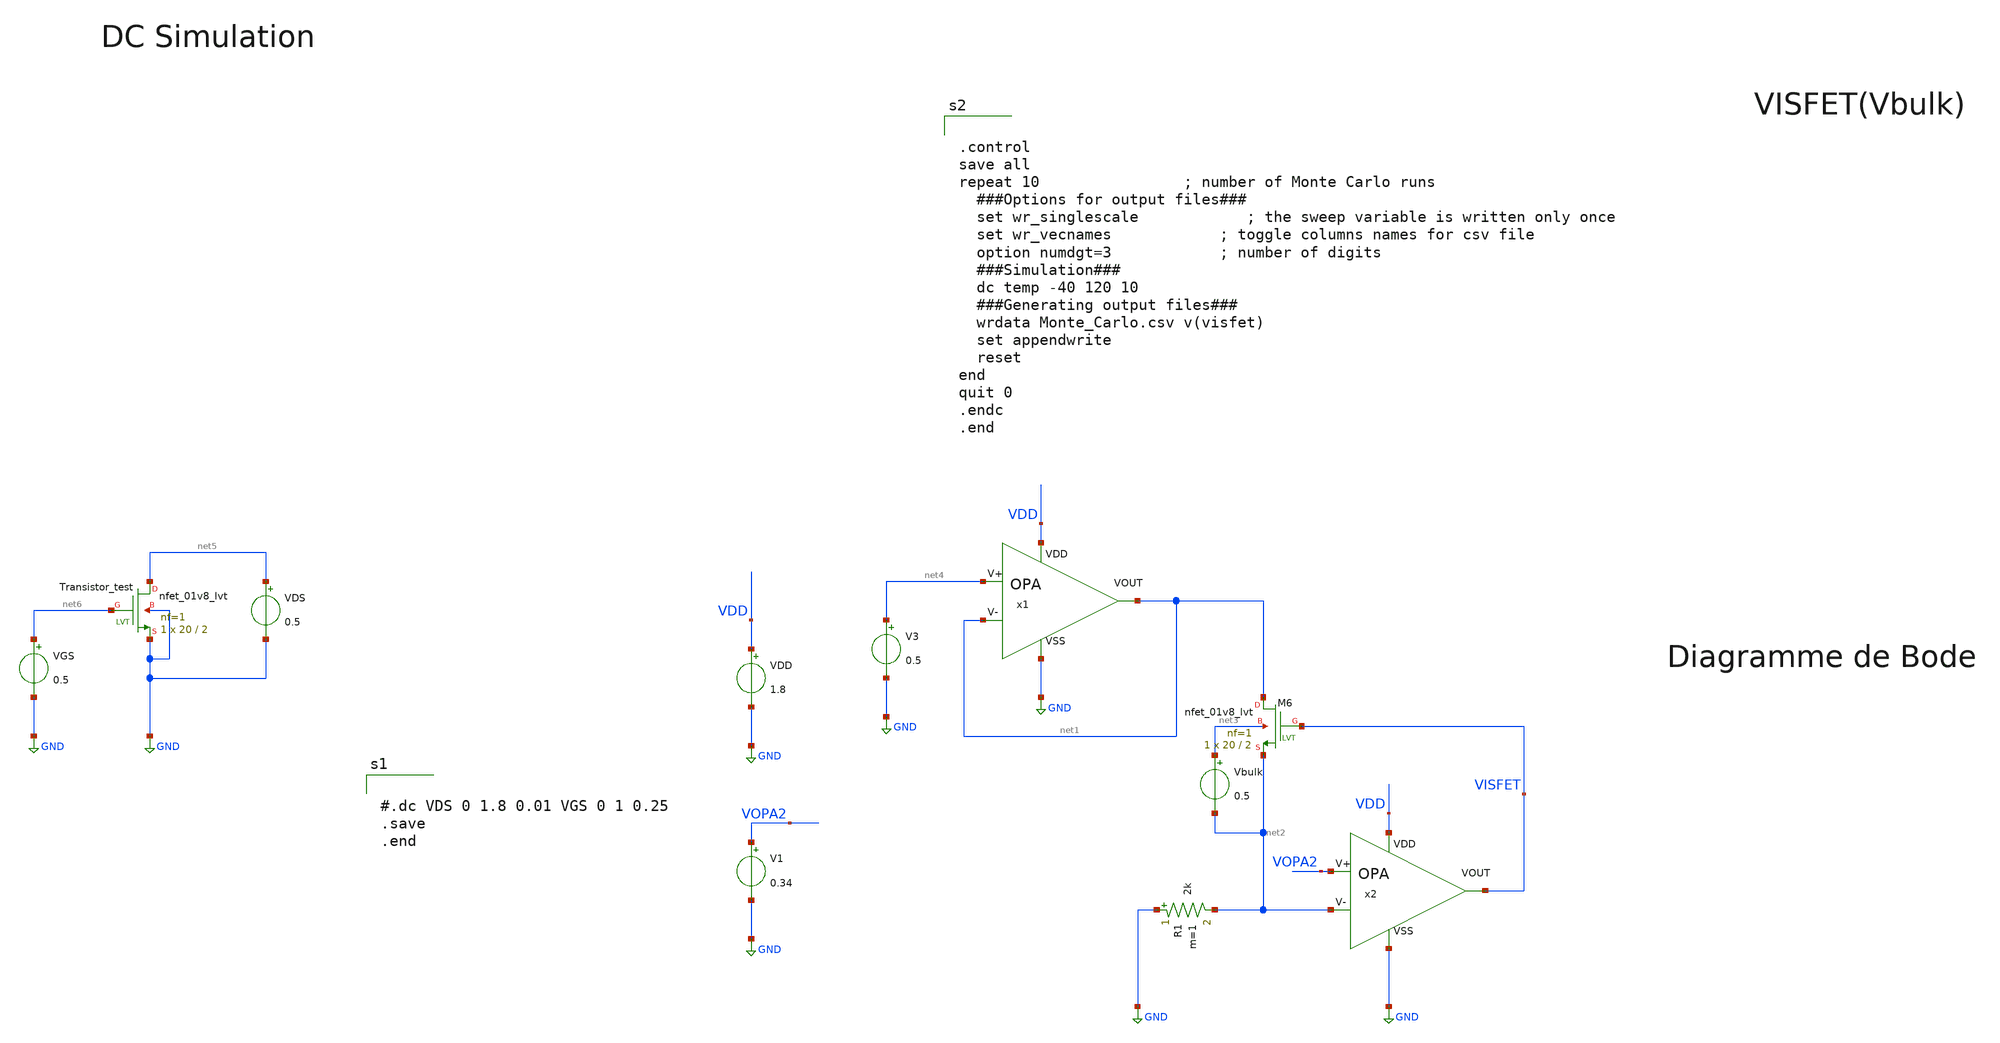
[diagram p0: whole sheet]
** sch_path: CVCC.sch
**.subckt CVCC
XM6 net1 VISFET net2 net3 sky130_fd_pr__nfet_01v8_lvt L=2 W=20 nf=1 ad='int((nf+1)/2) * W/nf * 0.29'
+ as='int((nf+2)/2) * W/nf * 0.29' pd='2*int((nf+1)/2) * (W/nf + 0.29)' ps='2*int((nf+2)/2) * (W/nf + 0.29)'
+ nrd='0.29 / W' nrs='0.29 / W' sa=0 sb=0 sd=0 mult=1 m=1
V1 VOPA2 GND 0.34
x1 VDD net4 net1 net1 GND OPA
x2 VDD VOPA2 net2 VISFET GND OPA
R1 GND net2 2k m=1
Vbulk net3 net2 0.5
VDD VDD GND 1.8
XTransistor_test net5 net6 GND GND sky130_fd_pr__nfet_01v8_lvt L=2 W=20 nf=1 ad='int((nf+1)/2) * W/nf * 0.29'
+ as='int((nf+2)/2) * W/nf * 0.29' pd='2*int((nf+1)/2) * (W/nf + 0.29)' ps='2*int((nf+2)/2) * (W/nf + 0.29)'
+ nrd='0.29 / W' nrs='0.29 / W' sa=0 sb=0 sd=0 mult=1 m=1
VDS net5 GND 0.5
VGS net6 GND 0.5
V3 net4 GND 0.5
**** begin user architecture code

** opencircuitdesign pdks install
.param MC_SWITCH=1.0
.lib $::SKYWATER_MODELS/sky130.lib.spice tt



#.dc VDS 0 1.8 0.01 VGS 0 1 0.25
.save
.end



.control
save all
repeat 10				; number of Monte Carlo runs
  ###Options for output files###
  set wr_singlescale			; the sweep variable is written only once
  set wr_vecnames			; toggle columns names for csv file
  option numdgt=3			; number of digits
  ###Simulation###
  dc temp -40 120 10
  ###Generating output files###
  wrdata Monte_Carlo.csv v(visfet)
  set appendwrite
  reset
end
quit 0
.endc
.end

**** end user architecture code
**.ends

* expanding   symbol:  OPA.sym # of pins=5
** sym_path: OPA.sym
** sch_path: OPA.sch
.subckt OPA VDD V+ V- VOUT VSS
*.ipin VSS
*.opin VOUT
*.ipin VDD
*.ipin V-
*.ipin V+
XM16 net5 net5 VDD VDD sky130_fd_pr__pfet_01v8_lvt L=2 W=39.5 nf=1 ad='int((nf+1)/2) * W/nf * 0.29' as='int((nf+2)/2) * W/nf * 0.29'
+ pd='2*int((nf+1)/2) * (W/nf + 0.29)' ps='2*int((nf+2)/2) * (W/nf + 0.29)' nrd='0.29 / W' nrs='0.29 / W'
+ sa=0 sb=0 sd=0 mult=1 m=1
XM17 net4 net4 net5 net5 sky130_fd_pr__pfet_01v8_lvt L=2 W=39.5 nf=1 ad='int((nf+1)/2) * W/nf * 0.29'
+ as='int((nf+2)/2) * W/nf * 0.29' pd='2*int((nf+1)/2) * (W/nf + 0.29)' ps='2*int((nf+2)/2) * (W/nf + 0.29)'
+ nrd='0.29 / W' nrs='0.29 / W' sa=0 sb=0 sd=0 mult=1 m=1
XM18 net4 net4 VSS VSS sky130_fd_pr__nfet_01v8_lvt L=2 W=6.67 nf=1 ad='int((nf+1)/2) * W/nf * 0.29' as='int((nf+2)/2) * W/nf * 0.29'
+ pd='2*int((nf+1)/2) * (W/nf + 0.29)' ps='2*int((nf+2)/2) * (W/nf + 0.29)' nrd='0.29 / W' nrs='0.29 / W'
+ sa=0 sb=0 sd=0 mult=1 m=1
XM19 net2 net4 VSS VSS sky130_fd_pr__nfet_01v8_lvt L=2 W=20 nf=1 ad='int((nf+1)/2) * W/nf * 0.29' as='int((nf+2)/2) * W/nf * 0.29'
+ pd='2*int((nf+1)/2) * (W/nf + 0.29)' ps='2*int((nf+2)/2) * (W/nf + 0.29)' nrd='0.29 / W' nrs='0.29 / W'
+ sa=0 sb=0 sd=0 mult=1 m=1
XM1 net1 V- net2 GND sky130_fd_pr__nfet_01v8_lvt L=2 W=10 nf=1 ad='int((nf+1)/2) * W/nf * 0.29' as='int((nf+2)/2) * W/nf * 0.29'
+ pd='2*int((nf+1)/2) * (W/nf + 0.29)' ps='2*int((nf+2)/2) * (W/nf + 0.29)' nrd='0.29 / W' nrs='0.29 / W'
+ sa=0 sb=0 sd=0 mult=1 m=1
XM2 net3 V+ net2 GND sky130_fd_pr__nfet_01v8_lvt L=2 W=10 nf=1 ad='int((nf+1)/2) * W/nf * 0.29' as='int((nf+2)/2) * W/nf * 0.29'
+ pd='2*int((nf+1)/2) * (W/nf + 0.29)' ps='2*int((nf+2)/2) * (W/nf + 0.29)' nrd='0.29 / W' nrs='0.29 / W'
+ sa=0 sb=0 sd=0 mult=1 m=1
XM3 net3 net1 VDD VDD sky130_fd_pr__pfet_01v8_lvt L=2 W=59.25 nf=1 ad='int((nf+1)/2) * W/nf * 0.29' as='int((nf+2)/2) * W/nf * 0.29'
+ pd='2*int((nf+1)/2) * (W/nf + 0.29)' ps='2*int((nf+2)/2) * (W/nf + 0.29)' nrd='0.29 / W' nrs='0.29 / W'
+ sa=0 sb=0 sd=0 mult=1 m=1
XM4 net1 net1 VDD VDD sky130_fd_pr__pfet_01v8_lvt L=2 W=59.25 nf=1 ad='int((nf+1)/2) * W/nf * 0.29' as='int((nf+2)/2) * W/nf * 0.29'
+ pd='2*int((nf+1)/2) * (W/nf + 0.29)' ps='2*int((nf+2)/2) * (W/nf + 0.29)' nrd='0.29 / W' nrs='0.29 / W'
+ sa=0 sb=0 sd=0 mult=1 m=1
XM20 net6 net4 VSS VSS sky130_fd_pr__nfet_01v8_lvt L=2 W=20 nf=1 ad='int((nf+1)/2) * W/nf * 0.29' as='int((nf+2)/2) * W/nf * 0.29'
+ pd='2*int((nf+1)/2) * (W/nf + 0.29)' ps='2*int((nf+2)/2) * (W/nf + 0.29)' nrd='0.29 / W' nrs='0.29 / W'
+ sa=0 sb=0 sd=0 mult=1 m=1
XM21 net6 net3 VDD VDD sky130_fd_pr__pfet_01v8_lvt L=2 W=118.5 nf=1 ad='int((nf+1)/2) * W/nf * 0.29'
+ as='int((nf+2)/2) * W/nf * 0.29' pd='2*int((nf+1)/2) * (W/nf + 0.29)' ps='2*int((nf+2)/2) * (W/nf + 0.29)'
+ nrd='0.29 / W' nrs='0.29 / W' sa=0 sb=0 sd=0 mult=1 m=1
XM22 VOUT net3 VDD VDD sky130_fd_pr__pfet_01v8_lvt L=2 W=118.5 nf=1 ad='int((nf+1)/2) * W/nf * 0.29'
+ as='int((nf+2)/2) * W/nf * 0.29' pd='2*int((nf+1)/2) * (W/nf + 0.29)' ps='2*int((nf+2)/2) * (W/nf + 0.29)'
+ nrd='0.29 / W' nrs='0.29 / W' sa=0 sb=0 sd=0 mult=1 m=1
XM23 VSS net6 VOUT VOUT sky130_fd_pr__pfet_01v8_lvt L=2 W=118.5 nf=1 ad='int((nf+1)/2) * W/nf * 0.29'
+ as='int((nf+2)/2) * W/nf * 0.29' pd='2*int((nf+1)/2) * (W/nf + 0.29)' ps='2*int((nf+2)/2) * (W/nf + 0.29)'
+ nrd='0.29 / W' nrs='0.29 / W' sa=0 sb=0 sd=0 mult=1 m=1
C1 net6 net7 2p m=1
R1 net3 net7 2k m=1
.ends

.GLOBAL GND
.end
